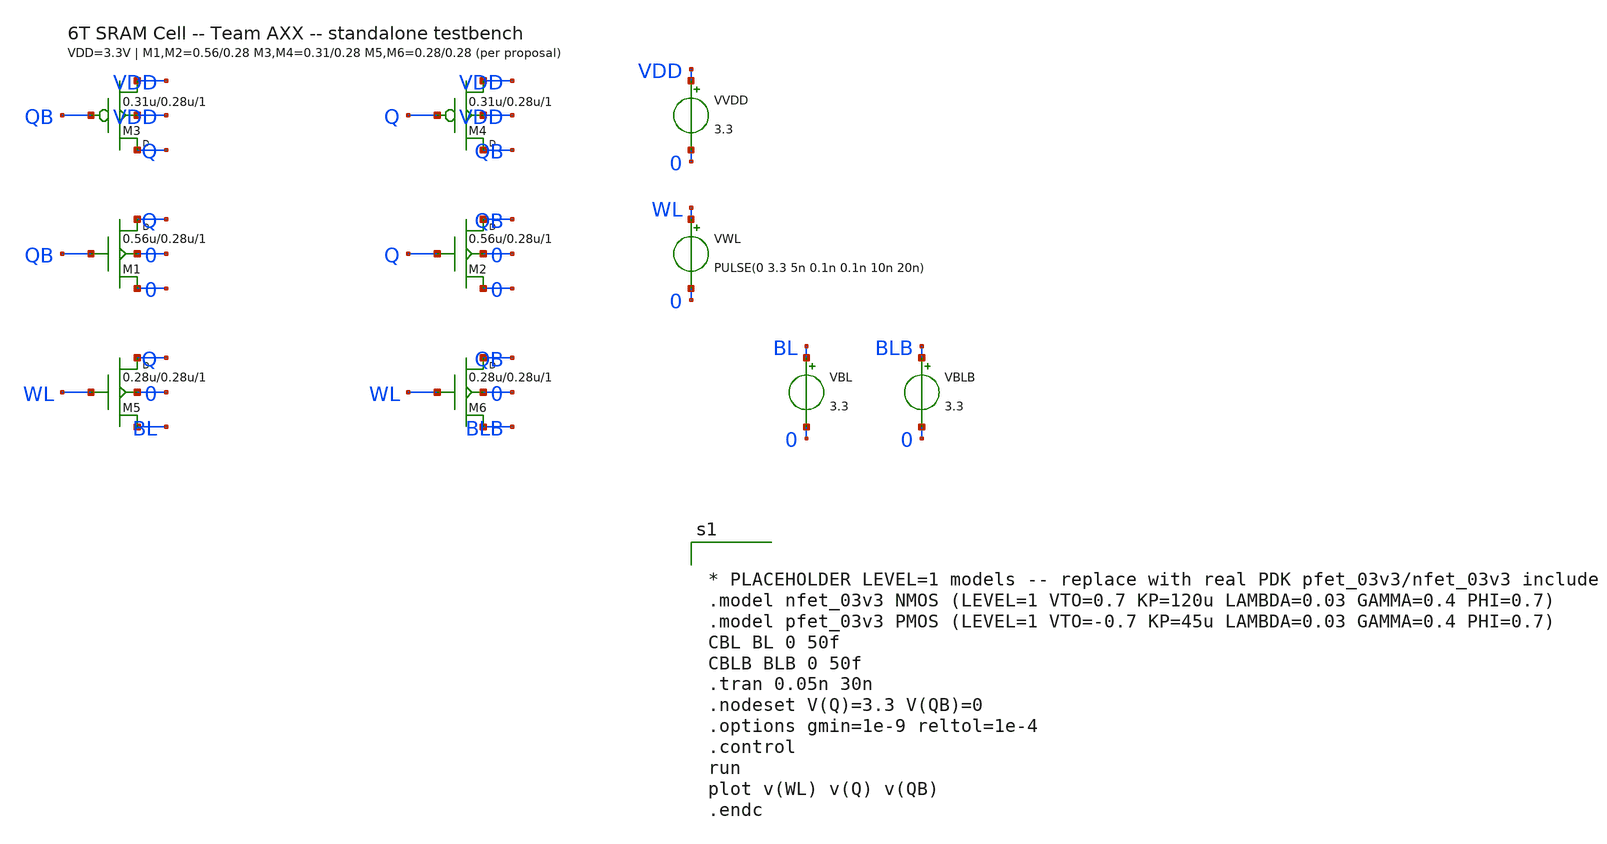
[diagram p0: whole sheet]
** sch_path: src/schematic/SRAM_6T/sram_6T_testbench.sch
**.subckt sram_6T_testbench
M3 Q QB VDD VDD pfet_03v3 w=0.31u l=0.28u m=1
M1 Q QB 0 0 nfet_03v3 w=0.56u l=0.28u m=1
M4 QB Q VDD VDD pfet_03v3 w=0.31u l=0.28u m=1
M2 QB Q 0 0 nfet_03v3 w=0.56u l=0.28u m=1
M5 Q WL BL 0 nfet_03v3 w=0.28u l=0.28u m=1
M6 QB WL BLB 0 nfet_03v3 w=0.28u l=0.28u m=1
VVDD VDD 0 3.3
VWL WL 0 PULSE(0 3.3 5n 0.1n 0.1n 10n 20n)
VBL BL 0 3.3
VBLB BLB 0 3.3
**** begin user architecture code


* PLACEHOLDER LEVEL=1 models -- replace with real PDK pfet_03v3/nfet_03v3 include
.model nfet_03v3 NMOS (LEVEL=1 VTO=0.7 KP=120u LAMBDA=0.03 GAMMA=0.4 PHI=0.7)
.model pfet_03v3 PMOS (LEVEL=1 VTO=-0.7 KP=45u LAMBDA=0.03 GAMMA=0.4 PHI=0.7)
CBL BL 0 50f
CBLB BLB 0 50f
.tran 0.05n 30n
.nodeset V(Q)=3.3 V(QB)=0
.options gmin=1e-9 reltol=1e-4
.control
run
plot v(WL) v(Q) v(QB)
.endc


**** end user architecture code
**.ends
.end
